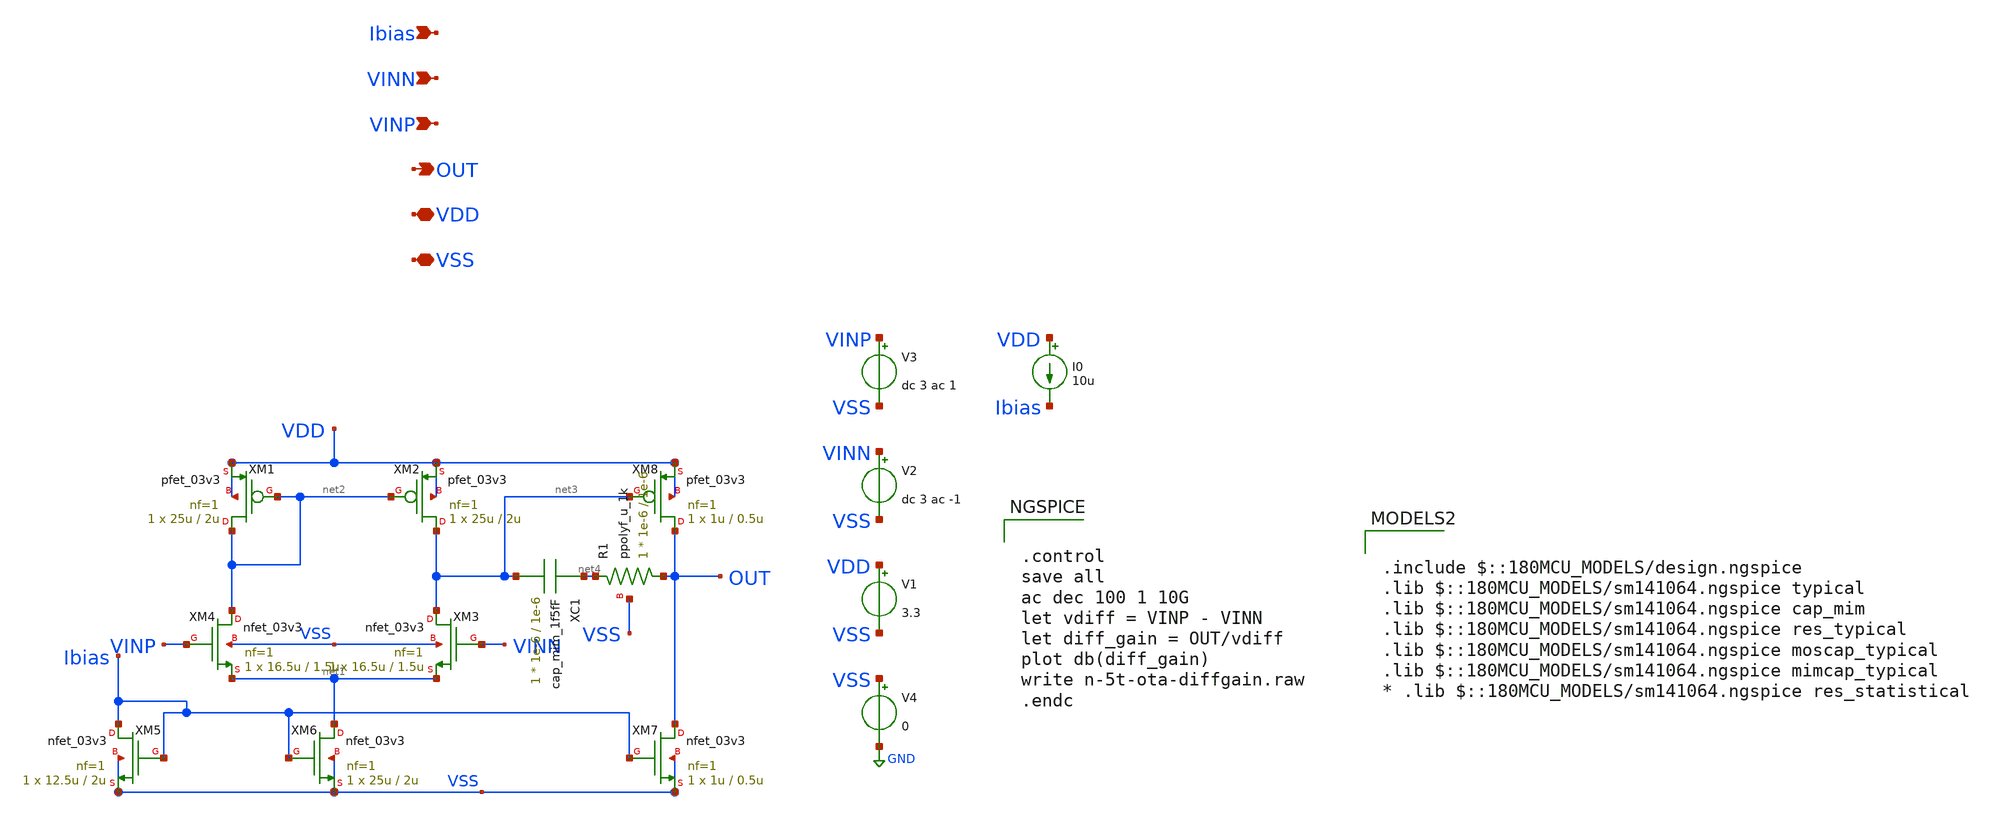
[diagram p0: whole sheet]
** sch_path: designs/libs/core_analog/nmos-ota.sch
**.subckt nmos-ota VINN VINP OUT VDD VSS Ibias
*.ipin VINN
*.ipin VINP
*.opin OUT
*.iopin VDD
*.iopin VSS
*.ipin Ibias
XM1 net2 net2 VDD VDD pfet_03v3 L=2u W=25u nf=1 ad='int((nf+1)/2) * W/nf * 0.18u' as='int((nf+2)/2) * W/nf * 0.18u'
+ pd='2*int((nf+1)/2) * (W/nf + 0.18u)' ps='2*int((nf+2)/2) * (W/nf + 0.18u)' nrd='0.18u / W' nrs='0.18u / W'
+ sa=0 sb=0 sd=0 m=1
XM2 net3 net2 VDD VDD pfet_03v3 L=2u W=25u nf=1 ad='int((nf+1)/2) * W/nf * 0.18u' as='int((nf+2)/2) * W/nf * 0.18u'
+ pd='2*int((nf+1)/2) * (W/nf + 0.18u)' ps='2*int((nf+2)/2) * (W/nf + 0.18u)' nrd='0.18u / W' nrs='0.18u / W'
+ sa=0 sb=0 sd=0 m=1
XM3 net3 VINN net1 VSS nfet_03v3 L=1.5u W=16.5u nf=1 ad='int((nf+1)/2) * W/nf * 0.18u' as='int((nf+2)/2) * W/nf * 0.18u'
+ pd='2*int((nf+1)/2) * (W/nf + 0.18u)' ps='2*int((nf+2)/2) * (W/nf + 0.18u)' nrd='0.18u / W' nrs='0.18u / W'
+ sa=0 sb=0 sd=0 m=1
XM4 net2 VINP net1 VSS nfet_03v3 L=1.5u W=16.5u nf=1 ad='int((nf+1)/2) * W/nf * 0.18u' as='int((nf+2)/2) * W/nf * 0.18u'
+ pd='2*int((nf+1)/2) * (W/nf + 0.18u)' ps='2*int((nf+2)/2) * (W/nf + 0.18u)' nrd='0.18u / W' nrs='0.18u / W'
+ sa=0 sb=0 sd=0 m=1
XM5 Ibias Ibias VSS VSS nfet_03v3 L=2u W=12.5u nf=1 ad='int((nf+1)/2) * W/nf * 0.18u' as='int((nf+2)/2) * W/nf * 0.18u'
+ pd='2*int((nf+1)/2) * (W/nf + 0.18u)' ps='2*int((nf+2)/2) * (W/nf + 0.18u)' nrd='0.18u / W' nrs='0.18u / W'
+ sa=0 sb=0 sd=0 m=1
XM6 net1 Ibias VSS VSS nfet_03v3 L=2u W=25u nf=1 ad='int((nf+1)/2) * W/nf * 0.18u' as='int((nf+2)/2) * W/nf * 0.18u'
+ pd='2*int((nf+1)/2) * (W/nf + 0.18u)' ps='2*int((nf+2)/2) * (W/nf + 0.18u)' nrd='0.18u / W' nrs='0.18u / W'
+ sa=0 sb=0 sd=0 m=1
XM7 OUT Ibias VSS VSS nfet_03v3 L=0.5u W=1u nf=1 ad='int((nf+1)/2) * W/nf * 0.18u' as='int((nf+2)/2) * W/nf * 0.18u'
+ pd='2*int((nf+1)/2) * (W/nf + 0.18u)' ps='2*int((nf+2)/2) * (W/nf + 0.18u)' nrd='0.18u / W' nrs='0.18u / W'
+ sa=0 sb=0 sd=0 m=1
XM8 OUT net3 VDD VDD pfet_03v3 L=0.5u W=1u nf=1 ad='int((nf+1)/2) * W/nf * 0.18u' as='int((nf+2)/2) * W/nf * 0.18u'
+ pd='2*int((nf+1)/2) * (W/nf + 0.18u)' ps='2*int((nf+2)/2) * (W/nf + 0.18u)' nrd='0.18u / W' nrs='0.18u / W'
+ sa=0 sb=0 sd=0 m=1
XC1 net4 net3 cap_mim_1f5fF c_width=1e-6 c_length=1e-6 m=1
XR1 OUT net4 VSS ppolyf_u_1k r_width=1e-6 r_length=1e-6 m=1
V1 VDD VSS 3.3
V2 VINN VSS dc 3 ac -1
V3 VINP VSS dc 3 ac 1
V4 VSS GND 0
I0 VDD Ibias 10u
**** begin user architecture code


.control
save all
ac dec 100 1 10G
let vdiff = VINP - VINN
let diff_gain = OUT/vdiff
plot db(diff_gain)
write n-5t-ota-diffgain.raw
.endc



.include $::180MCU_MODELS/design.ngspice
.lib $::180MCU_MODELS/sm141064.ngspice typical
.lib $::180MCU_MODELS/sm141064.ngspice cap_mim
.lib $::180MCU_MODELS/sm141064.ngspice res_typical
.lib $::180MCU_MODELS/sm141064.ngspice moscap_typical
.lib $::180MCU_MODELS/sm141064.ngspice mimcap_typical
* .lib $::180MCU_MODELS/sm141064.ngspice res_statistical

**** end user architecture code
**.ends
.GLOBAL GND
.end
